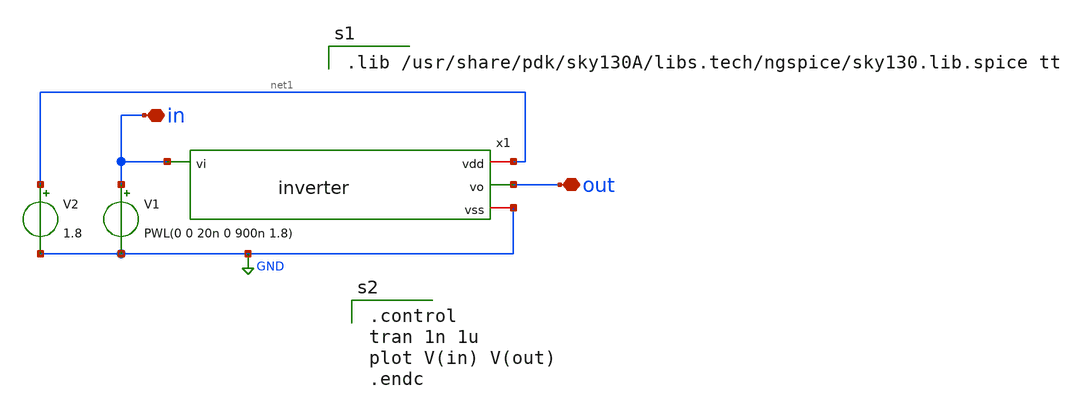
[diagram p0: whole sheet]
** sch_path: Day2_Lab/Day2_Lab/code/xschem/inverter_tb.sch
**.subckt inverter_tb in out
*.iopin in
*.iopin out
x1 net1 in out GND inverter
V1 in GND PWL(0 0 20n 0 900n 1.8)
V2 net1 GND 1.8
**** begin user architecture code

.lib /usr/share/pdk/sky130A/libs.tech/ngspice/sky130.lib.spice tt


.control
tran 1n 1u
plot V(in) V(out)
.endc

**** end user architecture code
**.ends
.GLOBAL GND
.end
